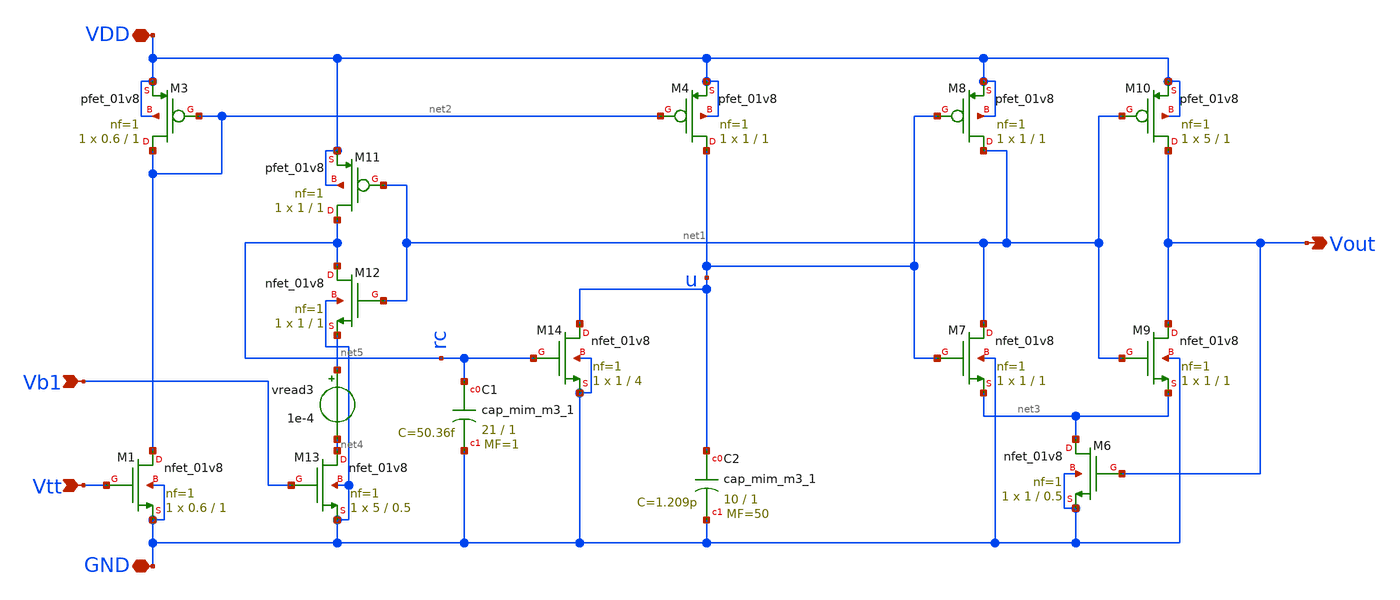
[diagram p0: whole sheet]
** sch_path: LIF_neuron/LIF_neuron_Vohra_modified.sch
**.subckt LIF_neuron_Vohra_modified Vtt GND Vb1 VDD Vout
*.ipin Vtt
*.iopin GND
*.ipin Vb1
*.iopin VDD
*.opin Vout
XM1 net2 Vtt GND GND sky130_fd_pr__nfet_01v8 L=1 W=0.6 nf=1 ad='int((nf+1)/2) * W/nf * 0.29' as='int((nf+2)/2) * W/nf * 0.29'
+ pd='2*int((nf+1)/2) * (W/nf + 0.29)' ps='2*int((nf+2)/2) * (W/nf + 0.29)' nrd='0.29 / W' nrs='0.29 / W'
+ sa=0 sb=0 sd=0 mult=1 m=1
XM3 net2 net2 VDD VDD sky130_fd_pr__pfet_01v8 L=1 W=0.6 nf=1 ad='int((nf+1)/2) * W/nf * 0.29' as='int((nf+2)/2) * W/nf * 0.29'
+ pd='2*int((nf+1)/2) * (W/nf + 0.29)' ps='2*int((nf+2)/2) * (W/nf + 0.29)' nrd='0.29 / W' nrs='0.29 / W'
+ sa=0 sb=0 sd=0 mult=1 m=1
XM13 net4 Vb1 GND GND sky130_fd_pr__nfet_01v8 L=0.5 W=5 nf=1 ad='int((nf+1)/2) * W/nf * 0.29' as='int((nf+2)/2) * W/nf * 0.29'
+ pd='2*int((nf+1)/2) * (W/nf + 0.29)' ps='2*int((nf+2)/2) * (W/nf + 0.29)' nrd='0.29 / W' nrs='0.29 / W'
+ sa=0 sb=0 sd=0 mult=1 m=1
XM12 rc net1 net5 GND sky130_fd_pr__nfet_01v8 L=1 W=1 nf=1 ad='int((nf+1)/2) * W/nf * 0.29' as='int((nf+2)/2) * W/nf * 0.29'
+ pd='2*int((nf+1)/2) * (W/nf + 0.29)' ps='2*int((nf+2)/2) * (W/nf + 0.29)' nrd='0.29 / W' nrs='0.29 / W'
+ sa=0 sb=0 sd=0 mult=1 m=1
XM11 rc net1 VDD VDD sky130_fd_pr__pfet_01v8 L=1 W=1 nf=1 ad='int((nf+1)/2) * W/nf * 0.29' as='int((nf+2)/2) * W/nf * 0.29'
+ pd='2*int((nf+1)/2) * (W/nf + 0.29)' ps='2*int((nf+2)/2) * (W/nf + 0.29)' nrd='0.29 / W' nrs='0.29 / W'
+ sa=0 sb=0 sd=0 mult=1 m=1
XC1 rc GND sky130_fd_pr__cap_mim_m3_1 W=21 L=1 MF=1 m=1
XM14 u rc GND GND sky130_fd_pr__nfet_01v8 L=4 W=1 nf=1 ad='int((nf+1)/2) * W/nf * 0.29' as='int((nf+2)/2) * W/nf * 0.29'
+ pd='2*int((nf+1)/2) * (W/nf + 0.29)' ps='2*int((nf+2)/2) * (W/nf + 0.29)' nrd='0.29 / W' nrs='0.29 / W'
+ sa=0 sb=0 sd=0 mult=1 m=1
XM4 u net2 VDD VDD sky130_fd_pr__pfet_01v8 L=1 W=1 nf=1 ad='int((nf+1)/2) * W/nf * 0.29' as='int((nf+2)/2) * W/nf * 0.29'
+ pd='2*int((nf+1)/2) * (W/nf + 0.29)' ps='2*int((nf+2)/2) * (W/nf + 0.29)' nrd='0.29 / W' nrs='0.29 / W'
+ sa=0 sb=0 sd=0 mult=1 m=1
XC2 u GND sky130_fd_pr__cap_mim_m3_1 W=10 L=1 MF=50 m=50
XM6 net3 Vout GND GND sky130_fd_pr__nfet_01v8 L=0.5 W=1 nf=1 ad='int((nf+1)/2) * W/nf * 0.29' as='int((nf+2)/2) * W/nf * 0.29'
+ pd='2*int((nf+1)/2) * (W/nf + 0.29)' ps='2*int((nf+2)/2) * (W/nf + 0.29)' nrd='0.29 / W' nrs='0.29 / W'
+ sa=0 sb=0 sd=0 mult=1 m=1
XM7 net1 u net3 GND sky130_fd_pr__nfet_01v8 L=1 W=1 nf=1 ad='int((nf+1)/2) * W/nf * 0.29' as='int((nf+2)/2) * W/nf * 0.29'
+ pd='2*int((nf+1)/2) * (W/nf + 0.29)' ps='2*int((nf+2)/2) * (W/nf + 0.29)' nrd='0.29 / W' nrs='0.29 / W'
+ sa=0 sb=0 sd=0 mult=1 m=1
XM8 net1 u VDD VDD sky130_fd_pr__pfet_01v8 L=1 W=1 nf=1 ad='int((nf+1)/2) * W/nf * 0.29' as='int((nf+2)/2) * W/nf * 0.29'
+ pd='2*int((nf+1)/2) * (W/nf + 0.29)' ps='2*int((nf+2)/2) * (W/nf + 0.29)' nrd='0.29 / W' nrs='0.29 / W'
+ sa=0 sb=0 sd=0 mult=1 m=1
XM9 Vout net1 net3 GND sky130_fd_pr__nfet_01v8 L=1 W=1 nf=1 ad='int((nf+1)/2) * W/nf * 0.29' as='int((nf+2)/2) * W/nf * 0.29'
+ pd='2*int((nf+1)/2) * (W/nf + 0.29)' ps='2*int((nf+2)/2) * (W/nf + 0.29)' nrd='0.29 / W' nrs='0.29 / W'
+ sa=0 sb=0 sd=0 mult=1 m=1
XM10 Vout net1 VDD VDD sky130_fd_pr__pfet_01v8 L=1 W=5 nf=1 ad='int((nf+1)/2) * W/nf * 0.29' as='int((nf+2)/2) * W/nf * 0.29'
+ pd='2*int((nf+1)/2) * (W/nf + 0.29)' ps='2*int((nf+2)/2) * (W/nf + 0.29)' nrd='0.29 / W' nrs='0.29 / W'
+ sa=0 sb=0 sd=0 mult=1 m=1
vread3 net5 net4 1e-4
**.ends
.end
